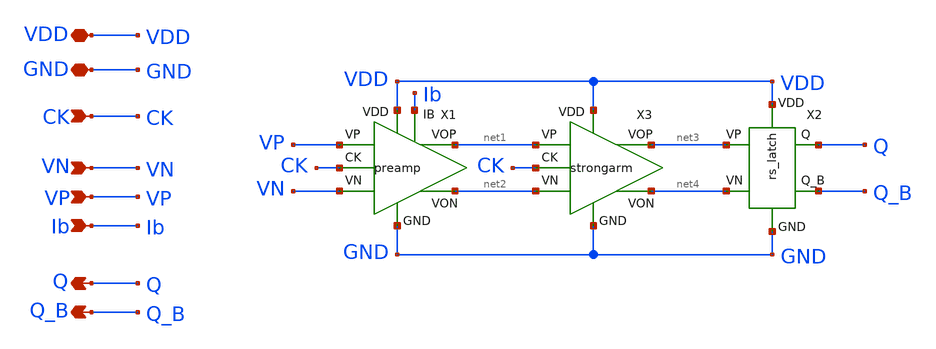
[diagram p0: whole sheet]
** sch_path: xschem/comparator/comparator.sch
**.subckt comparator VP VN VDD CK GND Q Q_B Ib
*.ipin VP
*.ipin VN
*.iopin VDD
*.ipin CK
*.iopin GND
*.opin Q
*.opin Q_B
*.ipin Ib
X1 VP VN GND net2 net1 VDD CK Ib preamp
X2 net3 net4 GND VDD Q Q_B rs_latch
X3 net1 net2 GND net4 net3 VDD CK strongarm
**.ends
.end
